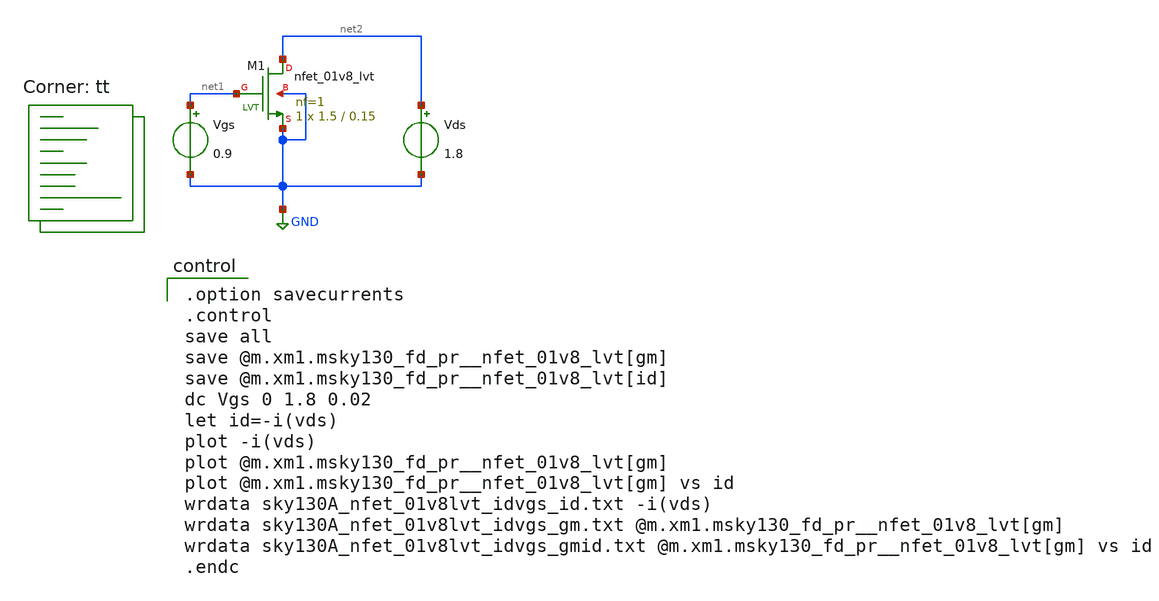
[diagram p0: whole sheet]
** sch_path: xschem/MOSFET/sky130A_nfet_01v8lvt_idvgs.sch
**.subckt sky130A_nfet_01v8lvt_idvgs
Vgs net1 GND 0.9
Vds net2 GND 1.8
XM1 net2 net1 GND GND sky130_fd_pr__nfet_01v8_lvt L=0.15 W=1.5 nf=1 ad='int((1 + 1)/2) * 1.5 / 1 * 0.29'
+ as='int((1 + 2)/2) * 1.5 / 1 * 0.29' pd='2*int((1 + 1)/2) * (1.5 / 1 + 0.29)' ps='2*int((1 + 2)/2) * (1.5 / 1 + 0.29)'
+ nrd='0.29 / 1.5 ' nrs='0.29 / 1.5 ' sa=0 sb=0 sd=0 mult=1 m=1
**** begin user architecture code

.option savecurrents
.control
save all
save @m.xm1.msky130_fd_pr__nfet_01v8_lvt[gm]
save @m.xm1.msky130_fd_pr__nfet_01v8_lvt[id]
dc Vgs 0 1.8 0.02
let id=-i(vds)
plot -i(vds)
plot @m.xm1.msky130_fd_pr__nfet_01v8_lvt[gm]
plot @m.xm1.msky130_fd_pr__nfet_01v8_lvt[gm] vs id
wrdata sky130A_nfet_01v8lvt_idvgs_id.txt -i(vds)
wrdata sky130A_nfet_01v8lvt_idvgs_gm.txt @m.xm1.msky130_fd_pr__nfet_01v8_lvt[gm]
wrdata sky130A_nfet_01v8lvt_idvgs_gmid.txt @m.xm1.msky130_fd_pr__nfet_01v8_lvt[gm] vs id
.endc

.lib $::SKYWATER_MODELS/sky130.lib.spice tt
**** end user architecture code
**.ends
.GLOBAL GND
.end
